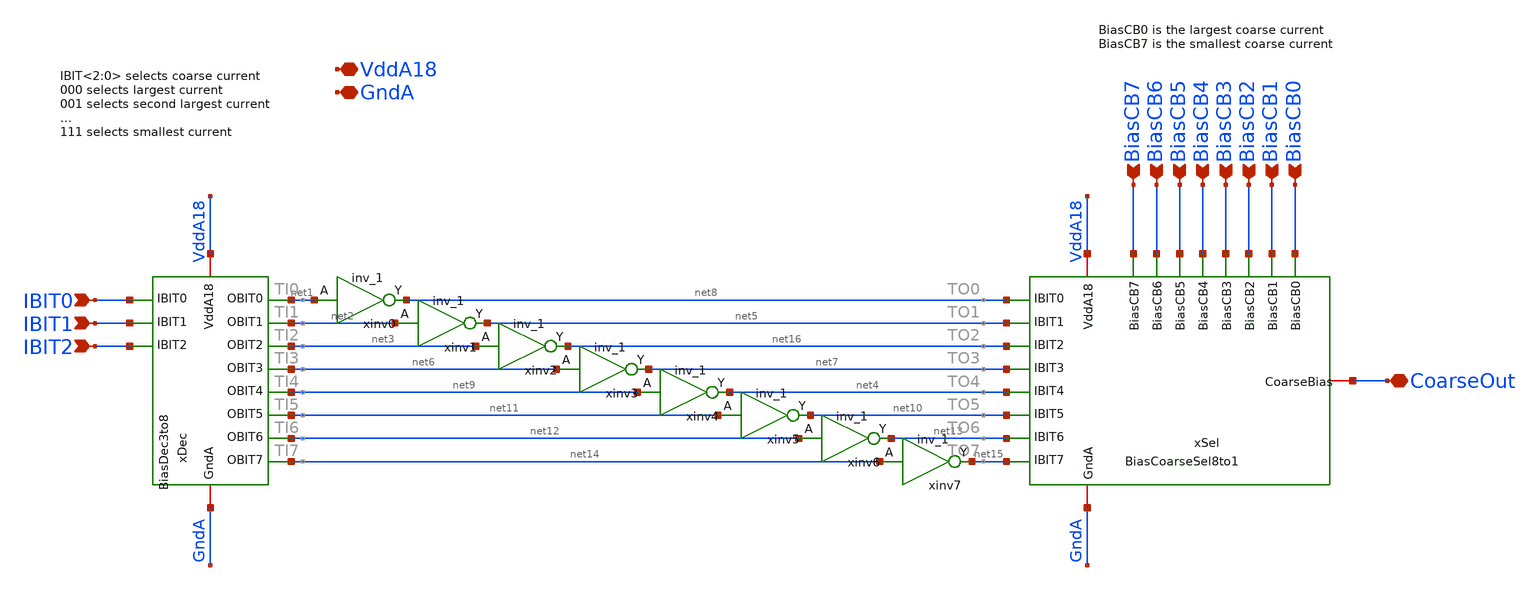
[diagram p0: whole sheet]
** sch_path: analog/xschem/BiasCoarseBuffer.sch
**.subckt BiasCoarseBuffer VddA18 GndA BiasCB7 BiasCB6 BiasCB5 BiasCB4 BiasCB3 BiasCB2 BiasCB1
*+ BiasCB0 IBIT0 IBIT1 IBIT2 CoarseOut
*.iopin VddA18
*.iopin GndA
*.ipin BiasCB7
*.ipin BiasCB6
*.ipin BiasCB5
*.ipin BiasCB4
*.ipin BiasCB3
*.ipin BiasCB2
*.ipin BiasCB1
*.ipin BiasCB0
*.ipin IBIT0
*.ipin IBIT1
*.ipin IBIT2
*.iopin CoarseOut
xSel VddA18 GndA net8 net5 net7 net4 net10 net13 net15 net16 BiasCB0 BiasCB1 BiasCB3 BiasCB4 BiasCB5
+ BiasCB6 BiasCB7 BiasCB2 CoarseOut BiasCoarseSel8to1
xDec VddA18 GndA net1 net2 net6 net9 net11 net12 net14 net3 IBIT0 IBIT1 IBIT2 BiasDec3to8
xinv0 net1 GndA GndA VddA18 VddA18 net8 sky130_fd_sc_hd__inv_1
xinv1 net2 GndA GndA VddA18 VddA18 net5 sky130_fd_sc_hd__inv_1
xinv2 net3 GndA GndA VddA18 VddA18 net16 sky130_fd_sc_hd__inv_1
xinv3 net6 GndA GndA VddA18 VddA18 net7 sky130_fd_sc_hd__inv_1
xinv4 net9 GndA GndA VddA18 VddA18 net4 sky130_fd_sc_hd__inv_1
xinv5 net11 GndA GndA VddA18 VddA18 net10 sky130_fd_sc_hd__inv_1
xinv6 net12 GndA GndA VddA18 VddA18 net13 sky130_fd_sc_hd__inv_1
xinv7 net14 GndA GndA VddA18 VddA18 net15 sky130_fd_sc_hd__inv_1
**.ends
.end
